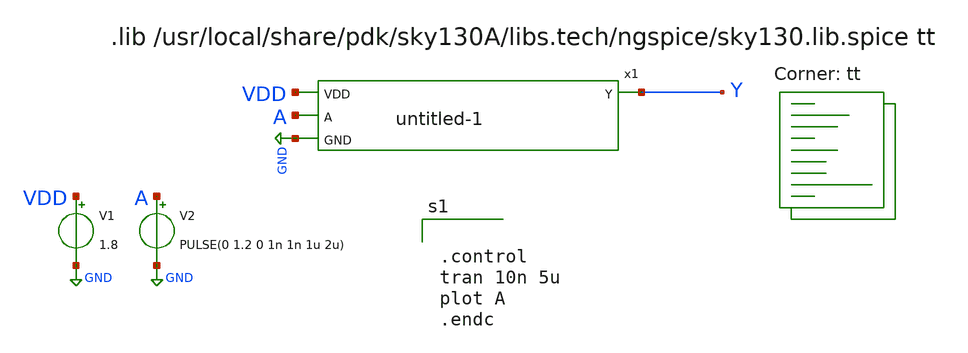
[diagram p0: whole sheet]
** sch_path: Work/work-1/untitled-2_tb.sch
**.subckt untitled-2_tb
x1 VDD A Y GND untitled-1
V1 VDD GND 1.8
V2 A GND PULSE(0 1.2 0 1n 1n 1u 2u)
**** begin user architecture code


.control
tran 10n 5u
plot A
.endc


.lib $::SKYWATER_MODELS/sky130.lib.spice tt
.lib /usr/local/share/pdk/sky130A/libs.tech/ngspice/sky130.lib.spice tt
**** end user architecture code
**.ends

* expanding   symbol:  untitled-1.sym # of pins=4
** sym_path: Work/work-1/untitled-1.sym
** sch_path: Work/work-1/untitled-1.sch
.subckt untitled-1 VDD A Y GND
*.ipin A
*.ipin VDD
*.ipin GND
*.opin Y
XM1 Y A GND GND sky130_fd_pr__nfet_01v8 L=0.15 W=1 nf=1 ad='int((1 + 1)/2) * 1 / 1 * 0.29' as='int((1 + 2)/2) * 1 / 1 * 0.29'
+ pd='2*int((1 + 1)/2) * (1 / 1 + 0.29)' ps='2*int((1 + 2)/2) * (1 / 1 + 0.29)' nrd='0.29 / 1 ' nrs='0.29 / 1 '
+ sa=0 sb=0 sd=0 mult=1 m=1
XM2 Y A VDD VDD sky130_fd_pr__pfet_01v8 L=0.15 W=1 nf=1 ad='int((1 + 1)/2) * 1 / 1 * 0.29' as='int((1 + 2)/2) * 1 / 1 * 0.29'
+ pd='2*int((1 + 1)/2) * (1 / 1 + 0.29)' ps='2*int((1 + 2)/2) * (1 / 1 + 0.29)' nrd='0.29 / 1 ' nrs='0.29 / 1 '
+ sa=0 sb=0 sd=0 mult=1 m=1
**** begin user architecture code
.lib /usr/local/share/pdk/sky130A/libs.tech/ngspice/sky130.lib.spice tt
**** end user architecture code
.ends

.GLOBAL GND
.end
